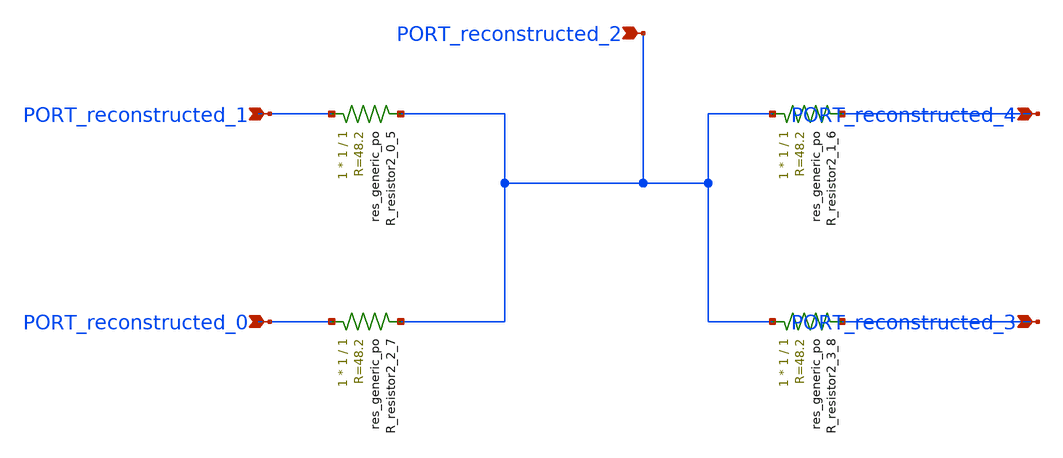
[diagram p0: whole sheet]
** sch_path: schematics/AMSNet/749.sch
**.subckt 749 PORT_reconstructed_0 PORT_reconstructed_1 PORT_reconstructed_3 PORT_reconstructed_4
*+ PORT_reconstructed_2
*.ipin PORT_reconstructed_0
*.ipin PORT_reconstructed_1
*.ipin PORT_reconstructed_3
*.ipin PORT_reconstructed_4
*.ipin PORT_reconstructed_2
XR_resistor2_0_5 PORT_reconstructed_1 PORT_reconstructed_2 sky130_fd_pr__res_generic_po W=1 L=1 m=1
XR_resistor2_1_6 PORT_reconstructed_2 PORT_reconstructed_4 sky130_fd_pr__res_generic_po W=1 L=1 m=1
XR_resistor2_2_7 PORT_reconstructed_0 PORT_reconstructed_2 sky130_fd_pr__res_generic_po W=1 L=1 m=1
XR_resistor2_3_8 PORT_reconstructed_2 PORT_reconstructed_3 sky130_fd_pr__res_generic_po W=1 L=1 m=1
**.ends
.end
